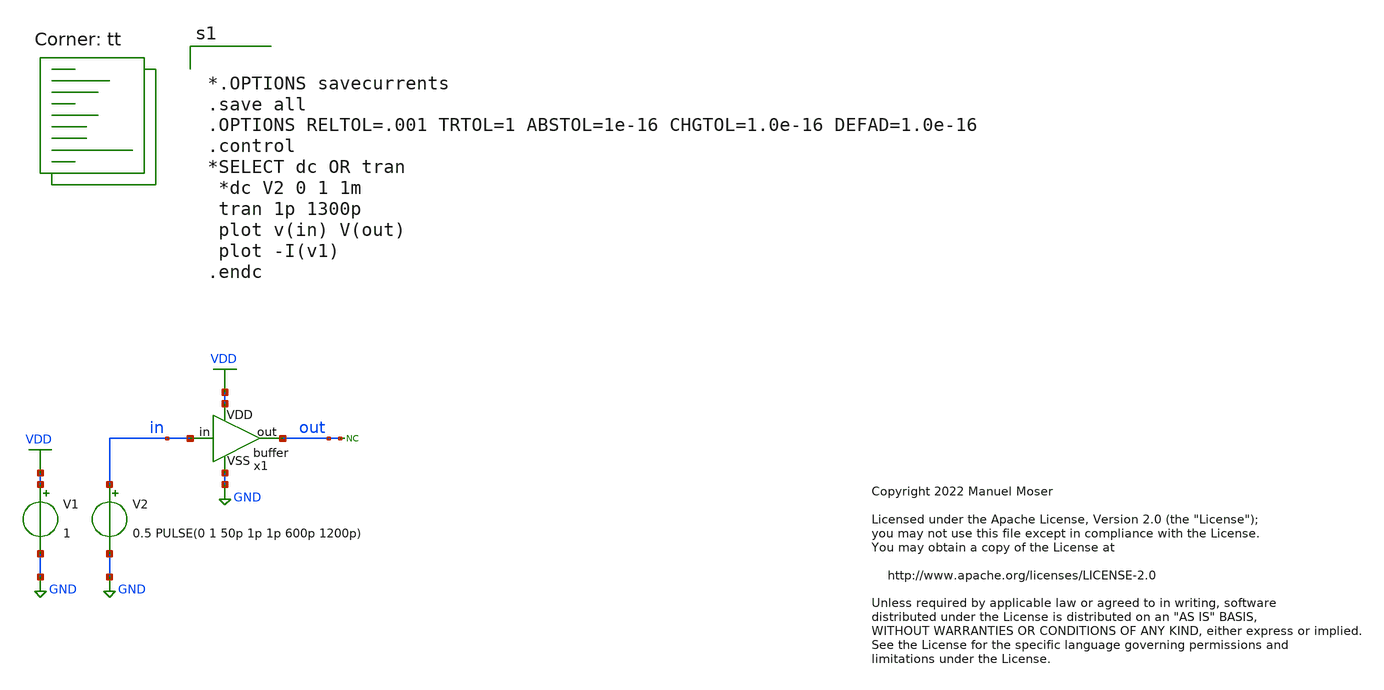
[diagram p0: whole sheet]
** sch_path: xschem/buffer/buffer_tb.sch
* Copyright 2022 Manuel Moser
* Licensed under the Apache License, Version 2.0 (the "License");
**.subckt buffer_tb
V1 VDD GND 1
V2 in GND 0.5 PULSE(0 1 50p 1p 1p 600p 1200p)
* noconn out
x1 VDD in out GND buffer
**** begin user architecture code


*.OPTIONS savecurrents
.save all
.OPTIONS RELTOL=.001 TRTOL=1 ABSTOL=1e-16 CHGTOL=1.0e-16 DEFAD=1.0e-16
.control
*SELECT dc OR tran
 *dc V2 0 1 1m
 tran 1p 1300p
 plot v(in) V(out)
 plot -I(v1)
.endc


.lib $::SKYWATER_MODELS/sky130.lib.spice tt
**** end user architecture code
**.ends
.GLOBAL GND
.GLOBAL VDD
.end
